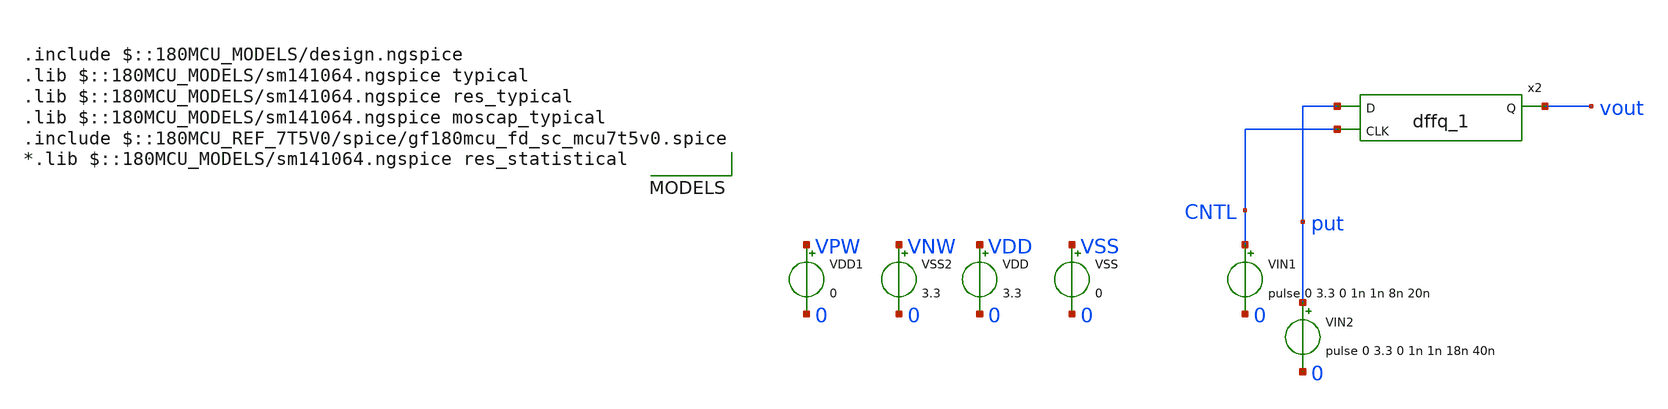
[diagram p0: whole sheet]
** sch_path: DAC/xschem/std_cell/tb_fiiles/Test_dffq_1.sch
**.subckt Test_dffq_1
VIN1 CNTL 0 pulse 0 3.3 0 1n 1n 8n 20n
VIN2 put 0 pulse 0 3.3 0 1n 1n 18n 40n
VDD VDD 0 3.3
VSS VSS 0 0
VDD1 VPW 0 0
VSS2 VNW 0 3.3
x2 put CNTL vout VDD VNW VPW VSS gf180mcu_fd_sc_mcu7t5v0__dffq_1
**** begin user architecture code

.include $::180MCU_MODELS/design.ngspice
.lib $::180MCU_MODELS/sm141064.ngspice typical
.lib $::180MCU_MODELS/sm141064.ngspice res_typical
.lib $::180MCU_MODELS/sm141064.ngspice moscap_typical
.include $::180MCU_REF_7T5V0/spice/gf180mcu_fd_sc_mcu7t5v0.spice
*.lib $::180MCU_MODELS/sm141064.ngspice res_statistical





.control
	tran 0.1n 5n
	plot v(CNTL) V(vout) V(put)
	plot v(vout)
	write test_and.raw

.endc
.save all




**** end user architecture code
**.ends
.end
